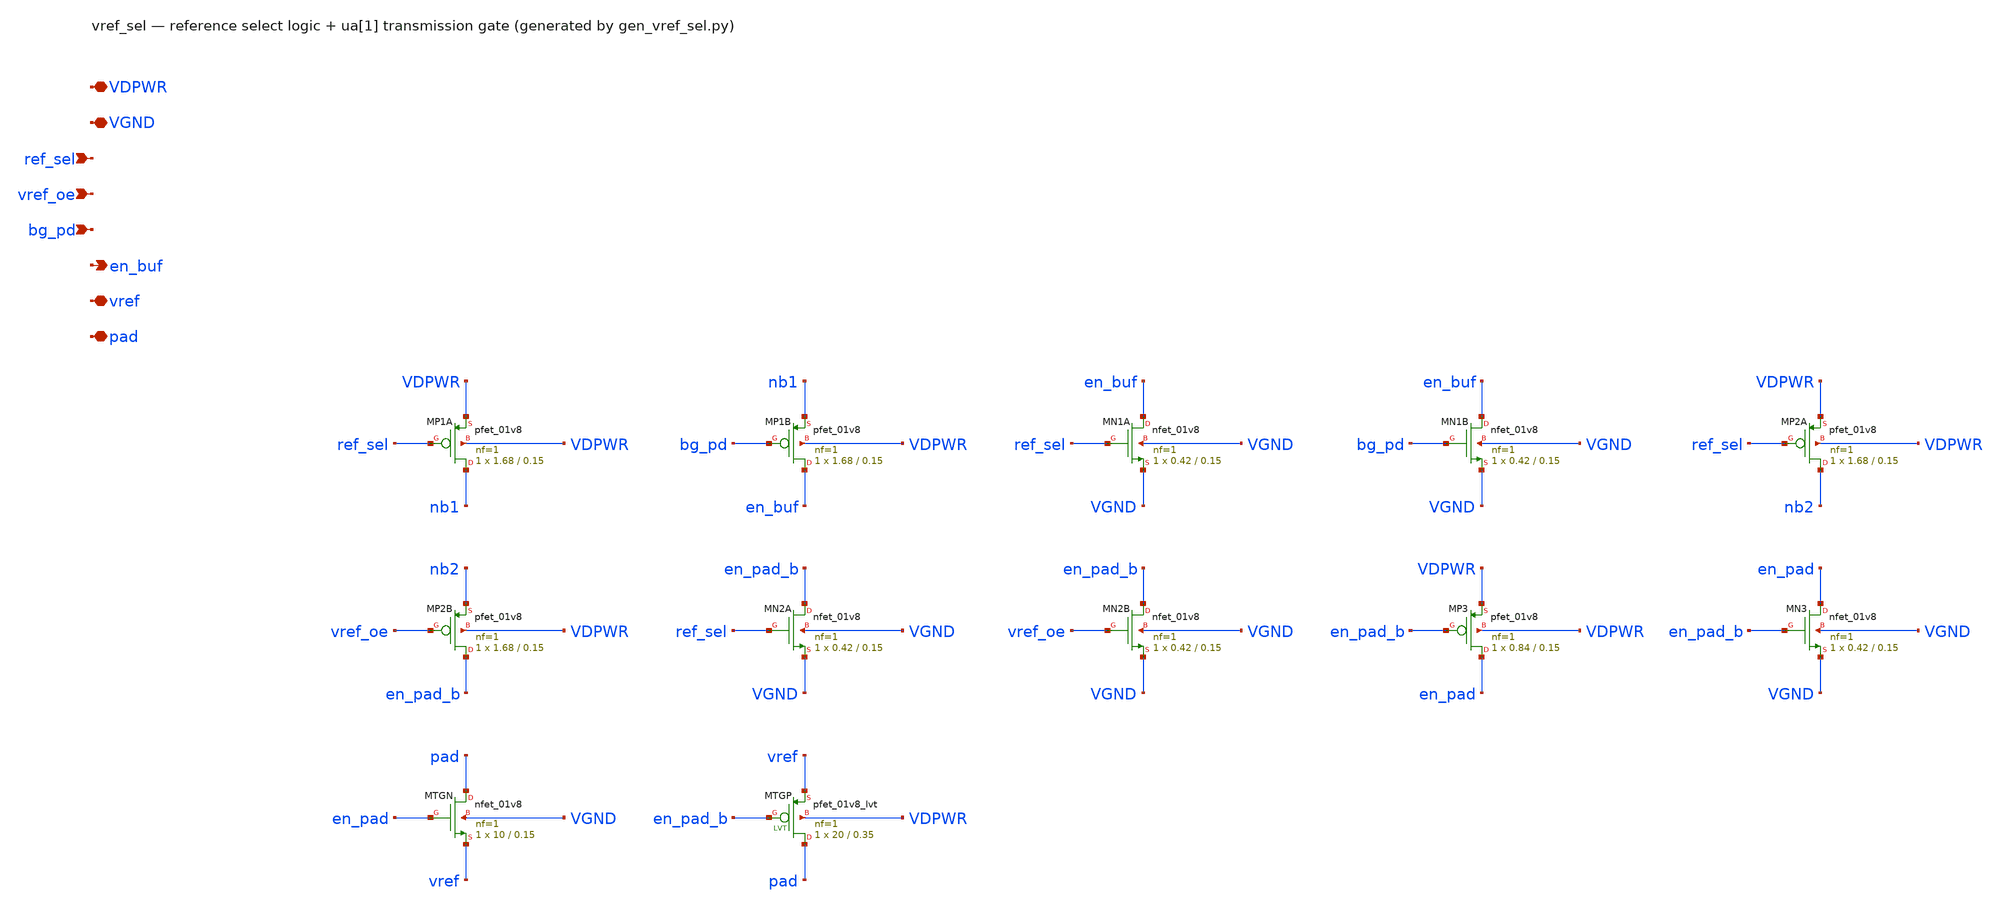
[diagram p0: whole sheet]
** sch_path: xschem/vref_sel.sch
**.subckt vref_sel VDPWR VGND ref_sel vref_oe bg_pd en_buf vref pad
*.iopin VDPWR
*.iopin VGND
*.ipin ref_sel
*.ipin vref_oe
*.ipin bg_pd
*.opin en_buf
*.iopin vref
*.iopin pad
XMP1A nb1 ref_sel VDPWR VDPWR sky130_fd_pr__pfet_01v8 L=0.15 W=1.68 nf=1 ad='int((nf+1)/2) * W/nf * 0.29'
+ as='int((nf+2)/2) * W/nf * 0.29' pd='2*int((nf+1)/2) * (W/nf + 0.29)' ps='2*int((nf+2)/2) * (W/nf + 0.29)'
+ nrd='0.29 / W' nrs='0.29 / W' sa=0 sb=0 sd=0 mult=1 m=1
XMP1B en_buf bg_pd nb1 VDPWR sky130_fd_pr__pfet_01v8 L=0.15 W=1.68 nf=1 ad='int((nf+1)/2) * W/nf * 0.29'
+ as='int((nf+2)/2) * W/nf * 0.29' pd='2*int((nf+1)/2) * (W/nf + 0.29)' ps='2*int((nf+2)/2) * (W/nf + 0.29)'
+ nrd='0.29 / W' nrs='0.29 / W' sa=0 sb=0 sd=0 mult=1 m=1
XMN1A en_buf ref_sel VGND VGND sky130_fd_pr__nfet_01v8 L=0.15 W=0.42 nf=1 ad='int((1 + 1)/2) * 0.42 / 1 * 0.29'
+ as='int((1 + 2)/2) * 0.42 / 1 * 0.29' pd='2*int((1 + 1)/2) * (0.42 / 1 + 0.29)' ps='2*int((1 + 2)/2) * (0.42 / 1 + 0.29)'
+ nrd='0.29 / 0.42 ' nrs='0.29 / 0.42 ' sa=0 sb=0 sd=0 mult=1 m=1
XMN1B en_buf bg_pd VGND VGND sky130_fd_pr__nfet_01v8 L=0.15 W=0.42 nf=1 ad='int((1 + 1)/2) * 0.42 / 1 * 0.29'
+ as='int((1 + 2)/2) * 0.42 / 1 * 0.29' pd='2*int((1 + 1)/2) * (0.42 / 1 + 0.29)' ps='2*int((1 + 2)/2) * (0.42 / 1 + 0.29)'
+ nrd='0.29 / 0.42 ' nrs='0.29 / 0.42 ' sa=0 sb=0 sd=0 mult=1 m=1
XMP2A nb2 ref_sel VDPWR VDPWR sky130_fd_pr__pfet_01v8 L=0.15 W=1.68 nf=1 ad='int((nf+1)/2) * W/nf * 0.29'
+ as='int((nf+2)/2) * W/nf * 0.29' pd='2*int((nf+1)/2) * (W/nf + 0.29)' ps='2*int((nf+2)/2) * (W/nf + 0.29)'
+ nrd='0.29 / W' nrs='0.29 / W' sa=0 sb=0 sd=0 mult=1 m=1
XMP2B en_pad_b vref_oe nb2 VDPWR sky130_fd_pr__pfet_01v8 L=0.15 W=1.68 nf=1 ad='int((nf+1)/2) * W/nf * 0.29'
+ as='int((nf+2)/2) * W/nf * 0.29' pd='2*int((nf+1)/2) * (W/nf + 0.29)' ps='2*int((nf+2)/2) * (W/nf + 0.29)'
+ nrd='0.29 / W' nrs='0.29 / W' sa=0 sb=0 sd=0 mult=1 m=1
XMN2A en_pad_b ref_sel VGND VGND sky130_fd_pr__nfet_01v8 L=0.15 W=0.42 nf=1 ad='int((1 + 1)/2) * 0.42 / 1 * 0.29'
+ as='int((1 + 2)/2) * 0.42 / 1 * 0.29' pd='2*int((1 + 1)/2) * (0.42 / 1 + 0.29)' ps='2*int((1 + 2)/2) * (0.42 / 1 + 0.29)'
+ nrd='0.29 / 0.42 ' nrs='0.29 / 0.42 ' sa=0 sb=0 sd=0 mult=1 m=1
XMN2B en_pad_b vref_oe VGND VGND sky130_fd_pr__nfet_01v8 L=0.15 W=0.42 nf=1 ad='int((1 + 1)/2) * 0.42 / 1 * 0.29'
+ as='int((1 + 2)/2) * 0.42 / 1 * 0.29' pd='2*int((1 + 1)/2) * (0.42 / 1 + 0.29)' ps='2*int((1 + 2)/2) * (0.42 / 1 + 0.29)'
+ nrd='0.29 / 0.42 ' nrs='0.29 / 0.42 ' sa=0 sb=0 sd=0 mult=1 m=1
XMP3 en_pad en_pad_b VDPWR VDPWR sky130_fd_pr__pfet_01v8 L=0.15 W=0.84 nf=1 ad='int((nf+1)/2) * W/nf * 0.29'
+ as='int((nf+2)/2) * W/nf * 0.29' pd='2*int((nf+1)/2) * (W/nf + 0.29)' ps='2*int((nf+2)/2) * (W/nf + 0.29)'
+ nrd='0.29 / W' nrs='0.29 / W' sa=0 sb=0 sd=0 mult=1 m=1
XMN3 en_pad en_pad_b VGND VGND sky130_fd_pr__nfet_01v8 L=0.15 W=0.42 nf=1 ad='int((1 + 1)/2) * 0.42 / 1 * 0.29'
+ as='int((1 + 2)/2) * 0.42 / 1 * 0.29' pd='2*int((1 + 1)/2) * (0.42 / 1 + 0.29)' ps='2*int((1 + 2)/2) * (0.42 / 1 + 0.29)'
+ nrd='0.29 / 0.42 ' nrs='0.29 / 0.42 ' sa=0 sb=0 sd=0 mult=1 m=1
XMTGN pad en_pad vref VGND sky130_fd_pr__nfet_01v8 L=0.15 W=10 nf=1 ad='int((1 + 1)/2) * 10 / 1 * 0.29'
+ as='int((1 + 2)/2) * 10 / 1 * 0.29' pd='2*int((1 + 1)/2) * (10 / 1 + 0.29)' ps='2*int((1 + 2)/2) * (10 / 1 + 0.29)'
+ nrd='0.29 / 10 ' nrs='0.29 / 10 ' sa=0 sb=0 sd=0 mult=1 m=1
XMTGP pad en_pad_b vref VDPWR sky130_fd_pr__pfet_01v8_lvt L=0.35 W=20 nf=1 ad='int((1 + 1)/2) * 20 / 1 * 0.29'
+ as='int((1 + 2)/2) * 20 / 1 * 0.29' pd='2*int((1 + 1)/2) * (20 / 1 + 0.29)' ps='2*int((1 + 2)/2) * (20 / 1 + 0.29)'
+ nrd='0.29 / 20 ' nrs='0.29 / 20 ' sa=0 sb=0 sd=0 mult=1 m=1
**.ends
.end
